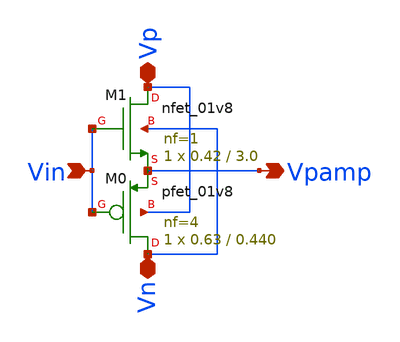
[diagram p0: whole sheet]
** sch_path: xschem/Vth_sch/Symbol/preamp1.sch
**.subckt preamp1 Vin Vpamp Vp Vn
*.ipin Vin
*.opin Vpamp
*.iopin Vp
*.iopin Vn
XM1 Vp Vin Vpamp Vn sky130_fd_pr__nfet_01v8 L=3.0 W=0.42 nf=1 ad='int((nf+1)/2) * W/nf * 0.29' as='int((nf+2)/2) * W/nf * 0.29'
+ pd='2*int((nf+1)/2) * (W/nf + 0.29)' ps='2*int((nf+2)/2) * (W/nf + 0.29)' nrd='0.29 / W' nrs='0.29 / W'
+ sa=0 sb=0 sd=0 mult=1 m=1
XM0 Vn Vin Vpamp Vp sky130_fd_pr__pfet_01v8 L=0.440 W=0.63 nf=4 ad='int((nf+1)/2) * W/nf * 0.29' as='int((nf+2)/2) * W/nf * 0.29'
+ pd='2*int((nf+1)/2) * (W/nf + 0.29)' ps='2*int((nf+2)/2) * (W/nf + 0.29)' nrd='0.29 / W' nrs='0.29 / W'
+ sa=0 sb=0 sd=0 mult=1 m=1
**.ends
.end
